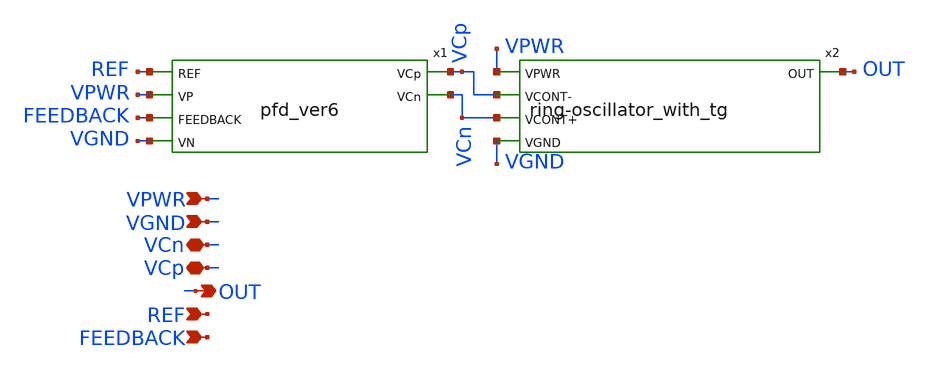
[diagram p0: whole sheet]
** sch_path: xschem_sch/pll.sch
**.subckt pll VPWR VGND OUT REF FEEDBACK VCn VCp
*.ipin VPWR
*.ipin VGND
*.opin OUT
*.ipin REF
*.ipin FEEDBACK
*.iopin VCn
*.iopin VCp
x1 REF VCp VCn VPWR FEEDBACK VGND pfd_ver6
x2 VPWR VCp OUT VCn VGND ring-oscillator_with_tg
**.ends

* expanding   symbol:  pfd_ver6.sym # of pins=6
** sym_path: xschem_sch/pfd_ver6.sym
** sch_path: xschem_sch/pfd_ver6.sch
.subckt pfd_ver6 REF VCp VCn VP FEEDBACK VN
*.opin VCn
*.ipin REF
*.ipin FEEDBACK
*.opin VCp
*.ipin VP
*.ipin VN
XM1 net1 REF VP VP sky130_fd_pr__pfet_01v8 L=0.15 W=0.45 nf=1 ad='int((nf+1)/2) * W/nf * 0.29' as='int((nf+2)/2) * W/nf * 0.29'
+ pd='2*int((nf+1)/2) * (W/nf + 0.29)' ps='2*int((nf+2)/2) * (W/nf + 0.29)' nrd='0.29 / W' nrs='0.29 / W'
+ sa=0 sb=0 sd=0 mult=1 m=1
XM2 net1 net2 VN VN sky130_fd_pr__nfet_01v8 L=0.15 W=0.45 nf=1 ad='int((nf+1)/2) * W/nf * 0.29' as='int((nf+2)/2) * W/nf * 0.29'
+ pd='2*int((nf+1)/2) * (W/nf + 0.29)' ps='2*int((nf+2)/2) * (W/nf + 0.29)' nrd='0.29 / W' nrs='0.29 / W'
+ sa=0 sb=0 sd=0 mult=1 m=1
XM3 net9 net1 VP VP sky130_fd_pr__pfet_01v8 L=0.15 W=0.45 nf=1 ad='int((nf+1)/2) * W/nf * 0.29' as='int((nf+2)/2) * W/nf * 0.29'
+ pd='2*int((nf+1)/2) * (W/nf + 0.29)' ps='2*int((nf+2)/2) * (W/nf + 0.29)' nrd='0.29 / W' nrs='0.29 / W'
+ sa=0 sb=0 sd=0 mult=1 m=1
XM4 net3 net9 VP VP sky130_fd_pr__pfet_01v8 L=0.15 W=0.45 nf=1 ad='int((nf+1)/2) * W/nf * 0.29' as='int((nf+2)/2) * W/nf * 0.29'
+ pd='2*int((nf+1)/2) * (W/nf + 0.29)' ps='2*int((nf+2)/2) * (W/nf + 0.29)' nrd='0.29 / W' nrs='0.29 / W'
+ sa=0 sb=0 sd=0 mult=1 m=1
XM5 net9 REF net8 VN sky130_fd_pr__nfet_01v8 L=0.15 W=0.45 nf=1 ad='int((nf+1)/2) * W/nf * 0.29' as='int((nf+2)/2) * W/nf * 0.29'
+ pd='2*int((nf+1)/2) * (W/nf + 0.29)' ps='2*int((nf+2)/2) * (W/nf + 0.29)' nrd='0.29 / W' nrs='0.29 / W'
+ sa=0 sb=0 sd=0 mult=1 m=1
XM6 net8 net1 VN VN sky130_fd_pr__nfet_01v8 L=0.15 W=0.45 nf=1 ad='int((nf+1)/2) * W/nf * 0.29' as='int((nf+2)/2) * W/nf * 0.29'
+ pd='2*int((nf+1)/2) * (W/nf + 0.29)' ps='2*int((nf+2)/2) * (W/nf + 0.29)' nrd='0.29 / W' nrs='0.29 / W'
+ sa=0 sb=0 sd=0 mult=1 m=1
XM7 net3 net9 VN VN sky130_fd_pr__nfet_01v8 L=0.15 W=0.45 nf=1 ad='int((nf+1)/2) * W/nf * 0.29' as='int((nf+2)/2) * W/nf * 0.29'
+ pd='2*int((nf+1)/2) * (W/nf + 0.29)' ps='2*int((nf+2)/2) * (W/nf + 0.29)' nrd='0.29 / W' nrs='0.29 / W'
+ sa=0 sb=0 sd=0 mult=1 m=1
XM8 net2 net4 net3 VP sky130_fd_pr__pfet_01v8 L=0.15 W=0.45 nf=1 ad='int((nf+1)/2) * W/nf * 0.29' as='int((nf+2)/2) * W/nf * 0.29'
+ pd='2*int((nf+1)/2) * (W/nf + 0.29)' ps='2*int((nf+2)/2) * (W/nf + 0.29)' nrd='0.29 / W' nrs='0.29 / W'
+ sa=0 sb=0 sd=0 mult=1 m=1
XM9 net2 net4 VN VN sky130_fd_pr__nfet_01v8 L=0.15 W=0.45 nf=1 ad='int((nf+1)/2) * W/nf * 0.29' as='int((nf+2)/2) * W/nf * 0.29'
+ pd='2*int((nf+1)/2) * (W/nf + 0.29)' ps='2*int((nf+2)/2) * (W/nf + 0.29)' nrd='0.29 / W' nrs='0.29 / W'
+ sa=0 sb=0 sd=0 mult=1 m=1
XM10 net5 net4 VP VP sky130_fd_pr__pfet_01v8 L=0.15 W=0.45 nf=1 ad='int((nf+1)/2) * W/nf * 0.29' as='int((nf+2)/2) * W/nf * 0.29'
+ pd='2*int((nf+1)/2) * (W/nf + 0.29)' ps='2*int((nf+2)/2) * (W/nf + 0.29)' nrd='0.29 / W' nrs='0.29 / W'
+ sa=0 sb=0 sd=0 mult=1 m=1
XM11 net5 net4 VN VN sky130_fd_pr__nfet_01v8 L=0.15 W=0.45 nf=1 ad='int((nf+1)/2) * W/nf * 0.29' as='int((nf+2)/2) * W/nf * 0.29'
+ pd='2*int((nf+1)/2) * (W/nf + 0.29)' ps='2*int((nf+2)/2) * (W/nf + 0.29)' nrd='0.29 / W' nrs='0.29 / W'
+ sa=0 sb=0 sd=0 mult=1 m=1
XM12 net4 net7 VP VP sky130_fd_pr__pfet_01v8 L=0.15 W=0.45 nf=1 ad='int((nf+1)/2) * W/nf * 0.29' as='int((nf+2)/2) * W/nf * 0.29'
+ pd='2*int((nf+1)/2) * (W/nf + 0.29)' ps='2*int((nf+2)/2) * (W/nf + 0.29)' nrd='0.29 / W' nrs='0.29 / W'
+ sa=0 sb=0 sd=0 mult=1 m=1
XM13 net4 FEEDBACK net6 VN sky130_fd_pr__nfet_01v8 L=0.15 W=0.45 nf=1 ad='int((nf+1)/2) * W/nf * 0.29'
+ as='int((nf+2)/2) * W/nf * 0.29' pd='2*int((nf+1)/2) * (W/nf + 0.29)' ps='2*int((nf+2)/2) * (W/nf + 0.29)'
+ nrd='0.29 / W' nrs='0.29 / W' sa=0 sb=0 sd=0 mult=1 m=1
XM14 net7 FEEDBACK VP VP sky130_fd_pr__pfet_01v8 L=0.15 W=0.45 nf=1 ad='int((nf+1)/2) * W/nf * 0.29'
+ as='int((nf+2)/2) * W/nf * 0.29' pd='2*int((nf+1)/2) * (W/nf + 0.29)' ps='2*int((nf+2)/2) * (W/nf + 0.29)'
+ nrd='0.29 / W' nrs='0.29 / W' sa=0 sb=0 sd=0 mult=1 m=1
XM15 net7 net2 VN VN sky130_fd_pr__nfet_01v8 L=0.15 W=0.45 nf=1 ad='int((nf+1)/2) * W/nf * 0.29' as='int((nf+2)/2) * W/nf * 0.29'
+ pd='2*int((nf+1)/2) * (W/nf + 0.29)' ps='2*int((nf+2)/2) * (W/nf + 0.29)' nrd='0.29 / W' nrs='0.29 / W'
+ sa=0 sb=0 sd=0 mult=1 m=1
XM16 net6 net7 VN VN sky130_fd_pr__nfet_01v8 L=0.15 W=0.45 nf=1 ad='int((nf+1)/2) * W/nf * 0.29' as='int((nf+2)/2) * W/nf * 0.29'
+ pd='2*int((nf+1)/2) * (W/nf + 0.29)' ps='2*int((nf+2)/2) * (W/nf + 0.29)' nrd='0.29 / W' nrs='0.29 / W'
+ sa=0 sb=0 sd=0 mult=1 m=1
XM45 VCp net5 VN VN sky130_fd_pr__nfet_01v8 L=0.15 W=0.45 nf=1 ad='int((nf+1)/2) * W/nf * 0.29' as='int((nf+2)/2) * W/nf * 0.29'
+ pd='2*int((nf+1)/2) * (W/nf + 0.29)' ps='2*int((nf+2)/2) * (W/nf + 0.29)' nrd='0.29 / W' nrs='0.29 / W'
+ sa=0 sb=0 sd=0 mult=1 m=1
XM44 VCp net11 VP VP sky130_fd_pr__pfet_01v8 L=0.15 W=0.45 nf=1 ad='int((nf+1)/2) * W/nf * 0.29' as='int((nf+2)/2) * W/nf * 0.29'
+ pd='2*int((nf+1)/2) * (W/nf + 0.29)' ps='2*int((nf+2)/2) * (W/nf + 0.29)' nrd='0.29 / W' nrs='0.29 / W'
+ sa=0 sb=0 sd=0 mult=1 m=1
XM17 VCn net3 VP VP sky130_fd_pr__pfet_01v8 L=0.15 W=0.45 nf=1 ad='int((nf+1)/2) * W/nf * 0.29' as='int((nf+2)/2) * W/nf * 0.29'
+ pd='2*int((nf+1)/2) * (W/nf + 0.29)' ps='2*int((nf+2)/2) * (W/nf + 0.29)' nrd='0.29 / W' nrs='0.29 / W'
+ sa=0 sb=0 sd=0 mult=1 m=1
XM18 VCn net10 VN VN sky130_fd_pr__nfet_01v8 L=0.15 W=0.45 nf=1 ad='int((nf+1)/2) * W/nf * 0.29' as='int((nf+2)/2) * W/nf * 0.29'
+ pd='2*int((nf+1)/2) * (W/nf + 0.29)' ps='2*int((nf+2)/2) * (W/nf + 0.29)' nrd='0.29 / W' nrs='0.29 / W'
+ sa=0 sb=0 sd=0 mult=1 m=1
XM19 net11 VN net9 VP sky130_fd_pr__pfet_01v8 L=0.15 W=0.45 nf=1 ad='int((nf+1)/2) * W/nf * 0.29' as='int((nf+2)/2) * W/nf * 0.29'
+ pd='2*int((nf+1)/2) * (W/nf + 0.29)' ps='2*int((nf+2)/2) * (W/nf + 0.29)' nrd='0.29 / W' nrs='0.29 / W'
+ sa=0 sb=0 sd=0 mult=1 m=1
XM20 net9 VP net11 VN sky130_fd_pr__nfet_01v8 L=0.15 W=0.45 nf=1 ad='int((nf+1)/2) * W/nf * 0.29' as='int((nf+2)/2) * W/nf * 0.29'
+ pd='2*int((nf+1)/2) * (W/nf + 0.29)' ps='2*int((nf+2)/2) * (W/nf + 0.29)' nrd='0.29 / W' nrs='0.29 / W'
+ sa=0 sb=0 sd=0 mult=1 m=1
XM21 net10 VN net4 VP sky130_fd_pr__pfet_01v8 L=0.15 W=0.45 nf=1 ad='int((nf+1)/2) * W/nf * 0.29' as='int((nf+2)/2) * W/nf * 0.29'
+ pd='2*int((nf+1)/2) * (W/nf + 0.29)' ps='2*int((nf+2)/2) * (W/nf + 0.29)' nrd='0.29 / W' nrs='0.29 / W'
+ sa=0 sb=0 sd=0 mult=1 m=1
XM22 net4 VP net10 VN sky130_fd_pr__nfet_01v8 L=0.15 W=0.45 nf=1 ad='int((nf+1)/2) * W/nf * 0.29' as='int((nf+2)/2) * W/nf * 0.29'
+ pd='2*int((nf+1)/2) * (W/nf + 0.29)' ps='2*int((nf+2)/2) * (W/nf + 0.29)' nrd='0.29 / W' nrs='0.29 / W'
+ sa=0 sb=0 sd=0 mult=1 m=1
.ends


* expanding   symbol:  ring-oscillator_with_tg.sym # of pins=5
** sym_path: xschem_sch/ring-oscillator_with_tg.sym
** sch_path: xschem_sch/ring-oscillator_with_tg.sch
.subckt ring-oscillator_with_tg VPWR VCONT- OUT VCONT+ VGND
*.ipin VPWR
*.opin OUT
*.ipin VGND
*.ipin VCONT+
*.ipin VCONT-
XM7 net1 net5 VPWR VPWR sky130_fd_pr__pfet_01v8 L=0.2 W=0.45 nf=1 ad='int((nf+1)/2) * W/nf * 0.29' as='int((nf+2)/2) * W/nf * 0.29'
+ pd='2*int((nf+1)/2) * (W/nf + 0.29)' ps='2*int((nf+2)/2) * (W/nf + 0.29)' nrd='0.29 / W' nrs='0.29 / W'
+ sa=0 sb=0 sd=0 mult=1 m=1
XM8 net3 VCONT- net1 VPWR sky130_fd_pr__pfet_01v8 L=0.2 W=0.45 nf=1 ad='int((nf+1)/2) * W/nf * 0.29'
+ as='int((nf+2)/2) * W/nf * 0.29' pd='2*int((nf+1)/2) * (W/nf + 0.29)' ps='2*int((nf+2)/2) * (W/nf + 0.29)'
+ nrd='0.29 / W' nrs='0.29 / W' sa=0 sb=0 sd=0 mult=1 m=1
XM9 net2 net3 VPWR VPWR sky130_fd_pr__pfet_01v8 L=0.2 W=0.45 nf=1 ad='int((nf+1)/2) * W/nf * 0.29' as='int((nf+2)/2) * W/nf * 0.29'
+ pd='2*int((nf+1)/2) * (W/nf + 0.29)' ps='2*int((nf+2)/2) * (W/nf + 0.29)' nrd='0.29 / W' nrs='0.29 / W'
+ sa=0 sb=0 sd=0 mult=1 m=1
XM11 OUT net4 VPWR VPWR sky130_fd_pr__pfet_01v8 L=0.2 W=0.45 nf=1 ad='int((nf+1)/2) * W/nf * 0.29' as='int((nf+2)/2) * W/nf * 0.29'
+ pd='2*int((nf+1)/2) * (W/nf + 0.29)' ps='2*int((nf+2)/2) * (W/nf + 0.29)' nrd='0.29 / W' nrs='0.29 / W'
+ sa=0 sb=0 sd=0 mult=1 m=1
XM10 net4 VCONT- net2 VPWR sky130_fd_pr__pfet_01v8 L=0.2 W=0.45 nf=1 ad='int((nf+1)/2) * W/nf * 0.29'
+ as='int((nf+2)/2) * W/nf * 0.29' pd='2*int((nf+1)/2) * (W/nf + 0.29)' ps='2*int((nf+2)/2) * (W/nf + 0.29)'
+ nrd='0.29 / W' nrs='0.29 / W' sa=0 sb=0 sd=0 mult=1 m=1
XM12 net5 VCONT- OUT VPWR sky130_fd_pr__pfet_01v8 L=0.2 W=0.45 nf=1 ad='int((nf+1)/2) * W/nf * 0.29'
+ as='int((nf+2)/2) * W/nf * 0.29' pd='2*int((nf+1)/2) * (W/nf + 0.29)' ps='2*int((nf+2)/2) * (W/nf + 0.29)'
+ nrd='0.29 / W' nrs='0.29 / W' sa=0 sb=0 sd=0 mult=1 m=1
XC1 VGND net5 sky130_fd_pr__cap_mim_m3_1 W=10 L=10 MF=1 m=1
XC2 VGND net3 sky130_fd_pr__cap_mim_m3_1 W=10 L=10 MF=1 m=1
XC3 VGND net4 sky130_fd_pr__cap_mim_m3_1 W=10 L=10 MF=10 m=10
XM13 OUT net4 VGND VGND sky130_fd_pr__nfet_01v8 L=0.2 W=0.45 nf=1 ad='int((nf+1)/2) * W/nf * 0.29' as='int((nf+2)/2) * W/nf * 0.29'
+ pd='2*int((nf+1)/2) * (W/nf + 0.29)' ps='2*int((nf+2)/2) * (W/nf + 0.29)' nrd='0.29 / W' nrs='0.29 / W'
+ sa=0 sb=0 sd=0 mult=1 m=1
XM1 net2 net3 VGND VGND sky130_fd_pr__nfet_01v8 L=0.2 W=0.45 nf=1 ad='int((nf+1)/2) * W/nf * 0.29' as='int((nf+2)/2) * W/nf * 0.29'
+ pd='2*int((nf+1)/2) * (W/nf + 0.29)' ps='2*int((nf+2)/2) * (W/nf + 0.29)' nrd='0.29 / W' nrs='0.29 / W'
+ sa=0 sb=0 sd=0 mult=1 m=1
XM2 net1 net5 VGND VGND sky130_fd_pr__nfet_01v8 L=0.2 W=0.45 nf=1 ad='int((nf+1)/2) * W/nf * 0.29' as='int((nf+2)/2) * W/nf * 0.29'
+ pd='2*int((nf+1)/2) * (W/nf + 0.29)' ps='2*int((nf+2)/2) * (W/nf + 0.29)' nrd='0.29 / W' nrs='0.29 / W'
+ sa=0 sb=0 sd=0 mult=1 m=1
XM3 OUT VCONT+ net5 VGND sky130_fd_pr__nfet_01v8 L=0.2 W=0.45 nf=1 ad='int((nf+1)/2) * W/nf * 0.29' as='int((nf+2)/2) * W/nf * 0.29'
+ pd='2*int((nf+1)/2) * (W/nf + 0.29)' ps='2*int((nf+2)/2) * (W/nf + 0.29)' nrd='0.29 / W' nrs='0.29 / W'
+ sa=0 sb=0 sd=0 mult=1 m=1
XM4 net1 VCONT+ net3 VGND sky130_fd_pr__nfet_01v8 L=0.2 W=0.45 nf=1 ad='int((nf+1)/2) * W/nf * 0.29'
+ as='int((nf+2)/2) * W/nf * 0.29' pd='2*int((nf+1)/2) * (W/nf + 0.29)' ps='2*int((nf+2)/2) * (W/nf + 0.29)'
+ nrd='0.29 / W' nrs='0.29 / W' sa=0 sb=0 sd=0 mult=1 m=1
XM5 net2 VCONT+ net4 VGND sky130_fd_pr__nfet_01v8 L=0.2 W=0.45 nf=1 ad='int((nf+1)/2) * W/nf * 0.29'
+ as='int((nf+2)/2) * W/nf * 0.29' pd='2*int((nf+1)/2) * (W/nf + 0.29)' ps='2*int((nf+2)/2) * (W/nf + 0.29)'
+ nrd='0.29 / W' nrs='0.29 / W' sa=0 sb=0 sd=0 mult=1 m=1
.ends

.end
